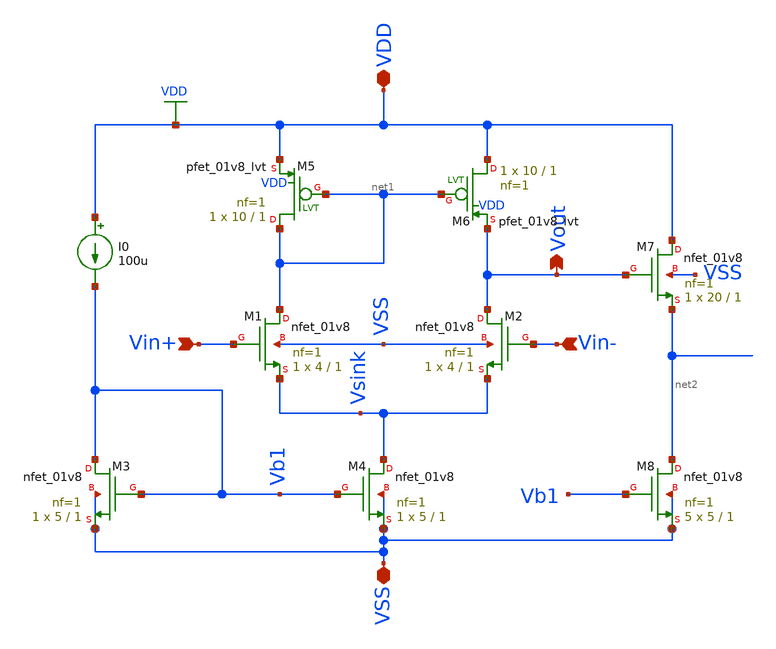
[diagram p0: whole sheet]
** sch_path: xschem/test/xschem/amplifiers/dec24/5TwithBuffer.sch
**.subckt 5TwithBuffer VDD VSS Vin- Vin+ Vout
*.iopin VDD
*.iopin VSS
*.ipin Vin-
*.ipin Vin+
*.opin Vout
I0 VDD Vb1 100u
XM1 net1 Vin+ Vsink VSS sky130_fd_pr__nfet_01v8 L=1 W=4 nf=1 ad='int((nf+1)/2) * W/nf * 0.29' as='int((nf+2)/2) * W/nf * 0.29'
+ pd='2*int((nf+1)/2) * (W/nf + 0.29)' ps='2*int((nf+2)/2) * (W/nf + 0.29)' nrd='0.29 / W' nrs='0.29 / W'
+ sa=0 sb=0 sd=0 mult=1 m=1
XM2 Vout Vin- Vsink VSS sky130_fd_pr__nfet_01v8 L=1 W=4 nf=1 ad='int((nf+1)/2) * W/nf * 0.29' as='int((nf+2)/2) * W/nf * 0.29'
+ pd='2*int((nf+1)/2) * (W/nf + 0.29)' ps='2*int((nf+2)/2) * (W/nf + 0.29)' nrd='0.29 / W' nrs='0.29 / W'
+ sa=0 sb=0 sd=0 mult=1 m=1
XM3 Vb1 Vb1 VSS VSS sky130_fd_pr__nfet_01v8 L=1 W=5 nf=1 ad='int((nf+1)/2) * W/nf * 0.29' as='int((nf+2)/2) * W/nf * 0.29'
+ pd='2*int((nf+1)/2) * (W/nf + 0.29)' ps='2*int((nf+2)/2) * (W/nf + 0.29)' nrd='0.29 / W' nrs='0.29 / W'
+ sa=0 sb=0 sd=0 mult=1 m=1
XM4 Vsink Vb1 VSS VSS sky130_fd_pr__nfet_01v8 L=1 W=5 nf=1 ad='int((nf+1)/2) * W/nf * 0.29' as='int((nf+2)/2) * W/nf * 0.29'
+ pd='2*int((nf+1)/2) * (W/nf + 0.29)' ps='2*int((nf+2)/2) * (W/nf + 0.29)' nrd='0.29 / W' nrs='0.29 / W'
+ sa=0 sb=0 sd=0 mult=1 m=1
XM7 VDD Vout net2 VSS sky130_fd_pr__nfet_01v8 L=1 W=20 nf=1 ad='int((nf+1)/2) * W/nf * 0.29' as='int((nf+2)/2) * W/nf * 0.29'
+ pd='2*int((nf+1)/2) * (W/nf + 0.29)' ps='2*int((nf+2)/2) * (W/nf + 0.29)' nrd='0.29 / W' nrs='0.29 / W'
+ sa=0 sb=0 sd=0 mult=1 m=1
XM8 net2 Vb1 VSS VSS sky130_fd_pr__nfet_01v8 L=1 W=5 nf=1 ad='int((nf+1)/2) * W/nf * 0.29' as='int((nf+2)/2) * W/nf * 0.29'
+ pd='2*int((nf+1)/2) * (W/nf + 0.29)' ps='2*int((nf+2)/2) * (W/nf + 0.29)' nrd='0.29 / W' nrs='0.29 / W'
+ sa=0 sb=0 sd=0 mult=5 m=5
XM5 net1 net1 VDD VDD sky130_fd_pr__pfet_01v8_lvt L=1 W=10 nf=1 ad='int((nf+1)/2) * W/nf * 0.29' as='int((nf+2)/2) * W/nf * 0.29'
+ pd='2*int((nf+1)/2) * (W/nf + 0.29)' ps='2*int((nf+2)/2) * (W/nf + 0.29)' nrd='0.29 / W' nrs='0.29 / W'
+ sa=0 sb=0 sd=0 mult=1 m=1
XM6 VDD net1 Vout VDD sky130_fd_pr__pfet_01v8_lvt L=1 W=10 nf=1 ad='int((nf+1)/2) * W/nf * 0.29' as='int((nf+2)/2) * W/nf * 0.29'
+ pd='2*int((nf+1)/2) * (W/nf + 0.29)' ps='2*int((nf+2)/2) * (W/nf + 0.29)' nrd='0.29 / W' nrs='0.29 / W'
+ sa=0 sb=0 sd=0 mult=1 m=1
**.ends
.GLOBAL VDD
.end
